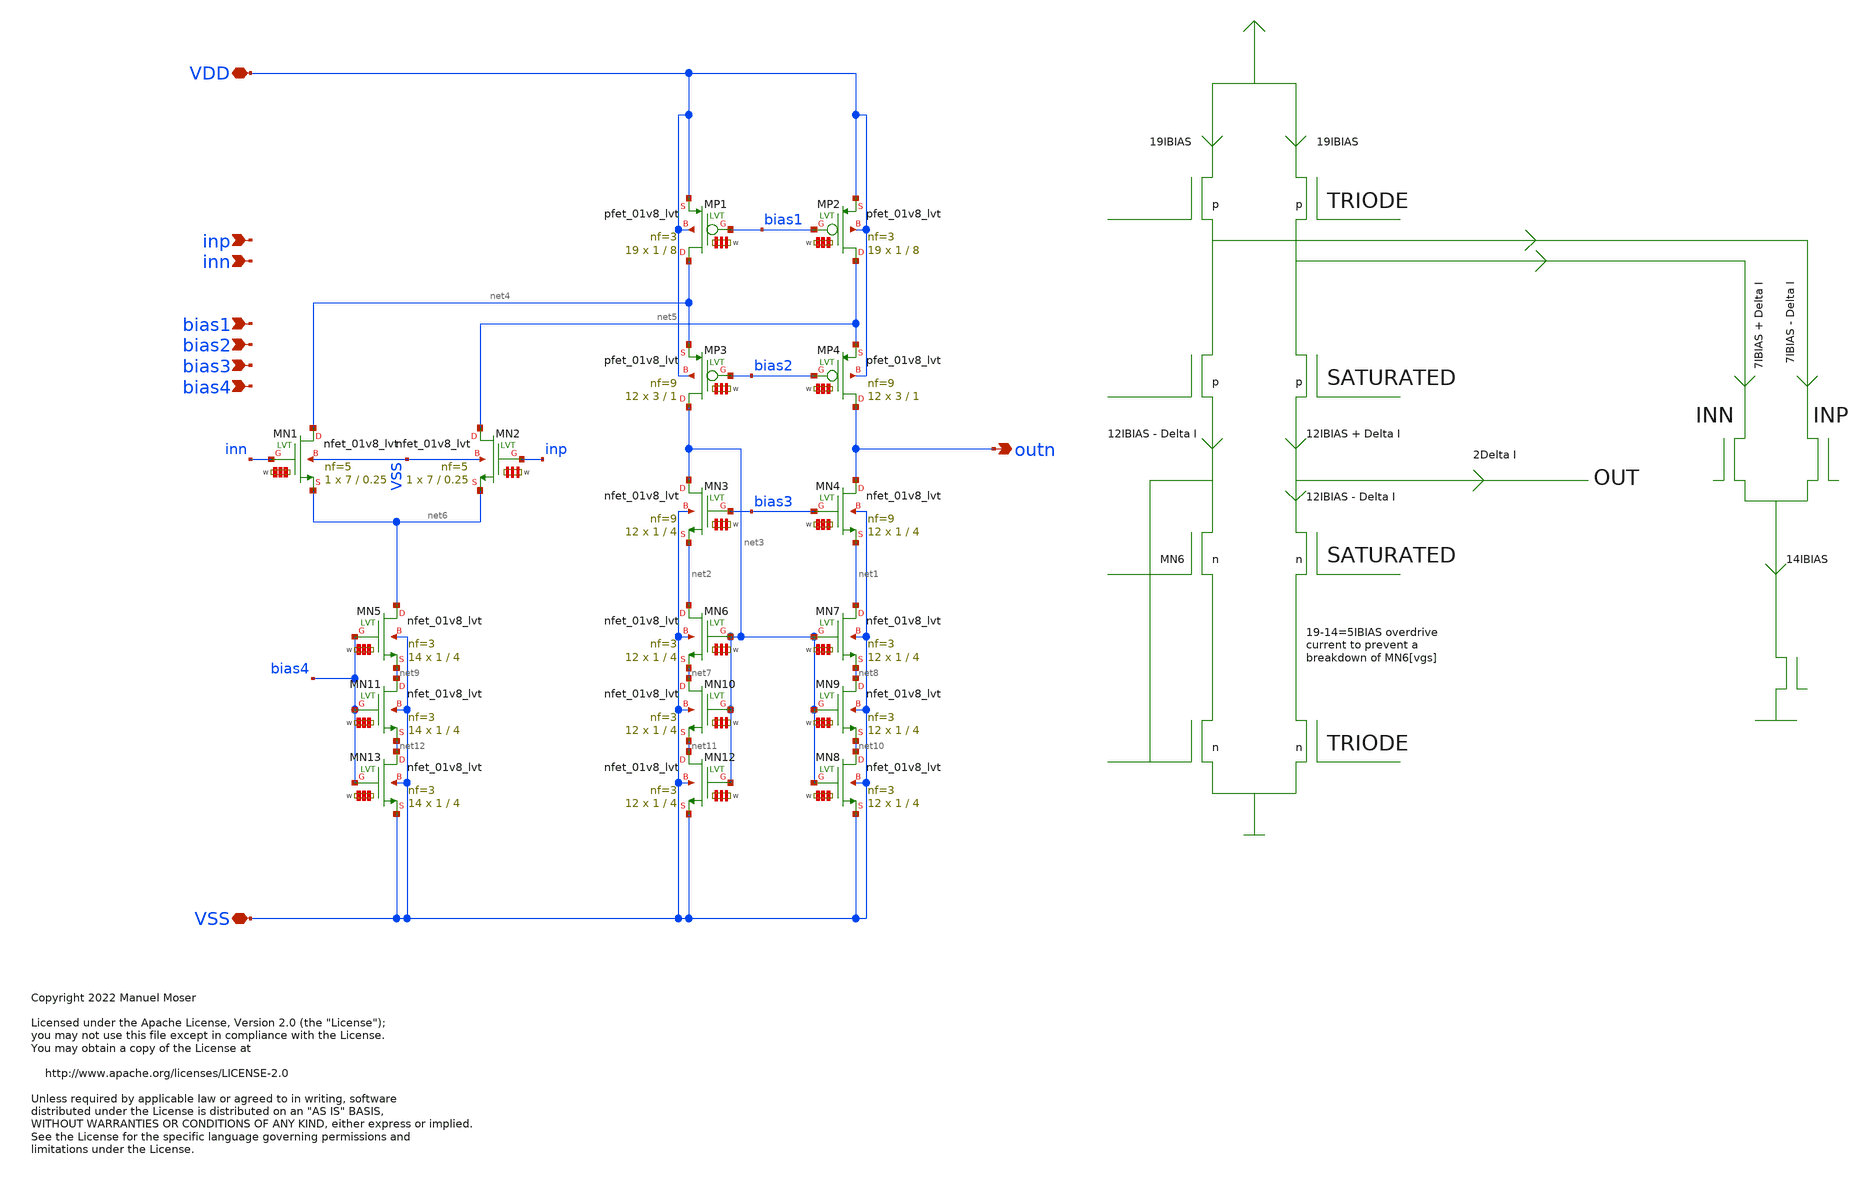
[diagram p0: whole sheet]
** sch_path: xschem/ldo_fc_n.sch
* Copyright 2022 Manuel Moser
* Licensed under the Apache License, Version 2.0 (the "License");
**.subckt ldo_fc_n VSS VDD inp inn bias1 outn bias2 bias3 bias4
*.iopin VSS
*.iopin VDD
*.ipin inp
*.ipin inn
*.ipin bias1
*.opin outn
*.ipin bias2
*.ipin bias3
*.ipin bias4
XMN4 outn bias3 net1 VSS sky130_fd_pr__nfet_01v8_lvt L=4 W='1 * 9 ' nf=9 ad='int((nf+1)/2) * W / nf * 0.29'
+ as='int((nf+2)/2) * W / nf * 0.29' pd='2*int((nf+1)/2) * (W / nf + 0.29)' ps='2*int((nf+2)/2) * (W / nf + 0.29)'
+ nrd='0.29 / W ' nrs='0.29 / W ' sa=0 sb=0 sd=0 mult=12 m=12
XMN7 net1 net3 net8 VSS sky130_fd_pr__nfet_01v8_lvt L=4 W='1 * 3 ' nf=3 ad='int((nf+1)/2) * W / nf * 0.29'
+ as='int((nf+2)/2) * W / nf * 0.29' pd='2*int((nf+1)/2) * (W / nf + 0.29)' ps='2*int((nf+2)/2) * (W / nf + 0.29)'
+ nrd='0.29 / W ' nrs='0.29 / W ' sa=0 sb=0 sd=0 mult=12 m=12
XMN3 net3 bias3 net2 VSS sky130_fd_pr__nfet_01v8_lvt L=4 W='1 * 9 ' nf=9 ad='int((nf+1)/2) * W / nf * 0.29'
+ as='int((nf+2)/2) * W / nf * 0.29' pd='2*int((nf+1)/2) * (W / nf + 0.29)' ps='2*int((nf+2)/2) * (W / nf + 0.29)'
+ nrd='0.29 / W ' nrs='0.29 / W ' sa=0 sb=0 sd=0 mult=12 m=12
XMN6 net2 net3 net7 VSS sky130_fd_pr__nfet_01v8_lvt L=4 W='1 * 3 ' nf=3 ad='int((nf+1)/2) * W / nf * 0.29'
+ as='int((nf+2)/2) * W / nf * 0.29' pd='2*int((nf+1)/2) * (W / nf + 0.29)' ps='2*int((nf+2)/2) * (W / nf + 0.29)'
+ nrd='0.29 / W ' nrs='0.29 / W ' sa=0 sb=0 sd=0 mult=12 m=12
XMP4 outn bias2 net5 VDD sky130_fd_pr__pfet_01v8_lvt L=1 W='3 * 9 ' nf=9 ad='int((nf+1)/2) * W / nf * 0.29'
+ as='int((nf+2)/2) * W / nf * 0.29' pd='2*int((nf+1)/2) * (W / nf + 0.29)' ps='2*int((nf+2)/2) * (W / nf + 0.29)'
+ nrd='0.29 / W ' nrs='0.29 / W ' sa=0 sb=0 sd=0 mult=12 m=12
XMP2 net5 bias1 VDD VDD sky130_fd_pr__pfet_01v8_lvt L=8 W='1 * 3 ' nf=3 ad='int((nf+1)/2) * W / nf * 0.29'
+ as='int((nf+2)/2) * W / nf * 0.29' pd='2*int((nf+1)/2) * (W / nf + 0.29)' ps='2*int((nf+2)/2) * (W / nf + 0.29)'
+ nrd='0.29 / W ' nrs='0.29 / W ' sa=0 sb=0 sd=0 mult=19 m=19
XMP3 net3 bias2 net4 VDD sky130_fd_pr__pfet_01v8_lvt L=1 W='3 * 9 ' nf=9 ad='int((nf+1)/2) * W / nf * 0.29'
+ as='int((nf+2)/2) * W / nf * 0.29' pd='2*int((nf+1)/2) * (W / nf + 0.29)' ps='2*int((nf+2)/2) * (W / nf + 0.29)'
+ nrd='0.29 / W ' nrs='0.29 / W ' sa=0 sb=0 sd=0 mult=12 m=12
XMP1 net4 bias1 VDD VDD sky130_fd_pr__pfet_01v8_lvt L=8 W='1 * 3 ' nf=3 ad='int((nf+1)/2) * W / nf * 0.29'
+ as='int((nf+2)/2) * W / nf * 0.29' pd='2*int((nf+1)/2) * (W / nf + 0.29)' ps='2*int((nf+2)/2) * (W / nf + 0.29)'
+ nrd='0.29 / W ' nrs='0.29 / W ' sa=0 sb=0 sd=0 mult=19 m=19
XMN5 net6 bias4 net9 VSS sky130_fd_pr__nfet_01v8_lvt L=4 W='1 * 3 ' nf=3 ad='int((nf+1)/2) * W / nf * 0.29'
+ as='int((nf+2)/2) * W / nf * 0.29' pd='2*int((nf+1)/2) * (W / nf + 0.29)' ps='2*int((nf+2)/2) * (W / nf + 0.29)'
+ nrd='0.29 / W ' nrs='0.29 / W ' sa=0 sb=0 sd=0 mult=14 m=14
XMN1 net4 inn net6 VSS sky130_fd_pr__nfet_01v8_lvt L=0.25 W='7 * 5 ' nf=5 ad='int((nf+1)/2) * W / nf * 0.29'
+ as='int((nf+2)/2) * W / nf * 0.29' pd='2*int((nf+1)/2) * (W / nf + 0.29)' ps='2*int((nf+2)/2) * (W / nf + 0.29)'
+ nrd='0.29 / W ' nrs='0.29 / W ' sa=0 sb=0 sd=0 mult=1 m=1
XMN2 net5 inp net6 VSS sky130_fd_pr__nfet_01v8_lvt L=0.25 W='7 * 5 ' nf=5 ad='int((nf+1)/2) * W / nf * 0.29'
+ as='int((nf+2)/2) * W / nf * 0.29' pd='2*int((nf+1)/2) * (W / nf + 0.29)' ps='2*int((nf+2)/2) * (W / nf + 0.29)'
+ nrd='0.29 / W ' nrs='0.29 / W ' sa=0 sb=0 sd=0 mult=1 m=1
XMN9 net8 net3 net10 VSS sky130_fd_pr__nfet_01v8_lvt L=4 W='1 * 3 ' nf=3 ad='int((nf+1)/2) * W / nf * 0.29'
+ as='int((nf+2)/2) * W / nf * 0.29' pd='2*int((nf+1)/2) * (W / nf + 0.29)' ps='2*int((nf+2)/2) * (W / nf + 0.29)'
+ nrd='0.29 / W ' nrs='0.29 / W ' sa=0 sb=0 sd=0 mult=12 m=12
XMN10 net7 net3 net11 VSS sky130_fd_pr__nfet_01v8_lvt L=4 W='1 * 3 ' nf=3 ad='int((nf+1)/2) * W / nf * 0.29'
+ as='int((nf+2)/2) * W / nf * 0.29' pd='2*int((nf+1)/2) * (W / nf + 0.29)' ps='2*int((nf+2)/2) * (W / nf + 0.29)'
+ nrd='0.29 / W ' nrs='0.29 / W ' sa=0 sb=0 sd=0 mult=12 m=12
XMN11 net9 bias4 net12 VSS sky130_fd_pr__nfet_01v8_lvt L=4 W='1 * 3 ' nf=3 ad='int((nf+1)/2) * W / nf * 0.29'
+ as='int((nf+2)/2) * W / nf * 0.29' pd='2*int((nf+1)/2) * (W / nf + 0.29)' ps='2*int((nf+2)/2) * (W / nf + 0.29)'
+ nrd='0.29 / W ' nrs='0.29 / W ' sa=0 sb=0 sd=0 mult=14 m=14
XMN8 net10 net3 VSS VSS sky130_fd_pr__nfet_01v8_lvt L=4 W='1 * 3 ' nf=3 ad='int((nf+1)/2) * W / nf * 0.29'
+ as='int((nf+2)/2) * W / nf * 0.29' pd='2*int((nf+1)/2) * (W / nf + 0.29)' ps='2*int((nf+2)/2) * (W / nf + 0.29)'
+ nrd='0.29 / W ' nrs='0.29 / W ' sa=0 sb=0 sd=0 mult=12 m=12
XMN12 net11 net3 VSS VSS sky130_fd_pr__nfet_01v8_lvt L=4 W='1 * 3 ' nf=3 ad='int((nf+1)/2) * W / nf * 0.29'
+ as='int((nf+2)/2) * W / nf * 0.29' pd='2*int((nf+1)/2) * (W / nf + 0.29)' ps='2*int((nf+2)/2) * (W / nf + 0.29)'
+ nrd='0.29 / W ' nrs='0.29 / W ' sa=0 sb=0 sd=0 mult=12 m=12
XMN13 net12 bias4 VSS VSS sky130_fd_pr__nfet_01v8_lvt L=4 W='1 * 3 ' nf=3 ad='int((nf+1)/2) * W / nf * 0.29'
+ as='int((nf+2)/2) * W / nf * 0.29' pd='2*int((nf+1)/2) * (W / nf + 0.29)' ps='2*int((nf+2)/2) * (W / nf + 0.29)'
+ nrd='0.29 / W ' nrs='0.29 / W ' sa=0 sb=0 sd=0 mult=14 m=14
**.ends
.end
